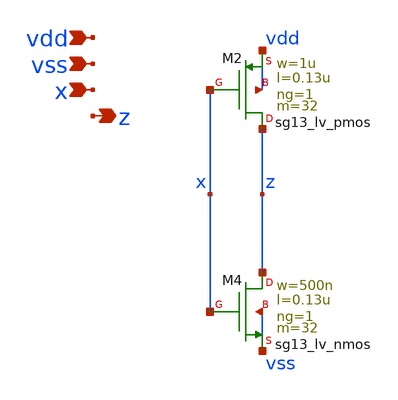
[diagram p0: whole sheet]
** sch_path: MSPHY9932-main/schematic/xschem/buf_32.sch
**.subckt buf_32 vdd vss x z
*.ipin vdd
*.ipin vss
*.ipin x
*.opin z
XM2 z x vdd vdd sg13_lv_pmos w=1u l=0.13u ng=1 m=32 mm_ok=1
XM4 z x vss vss sg13_lv_nmos w=500n l=0.13u ng=1 m=32 mm_ok=1
**.ends
.end
